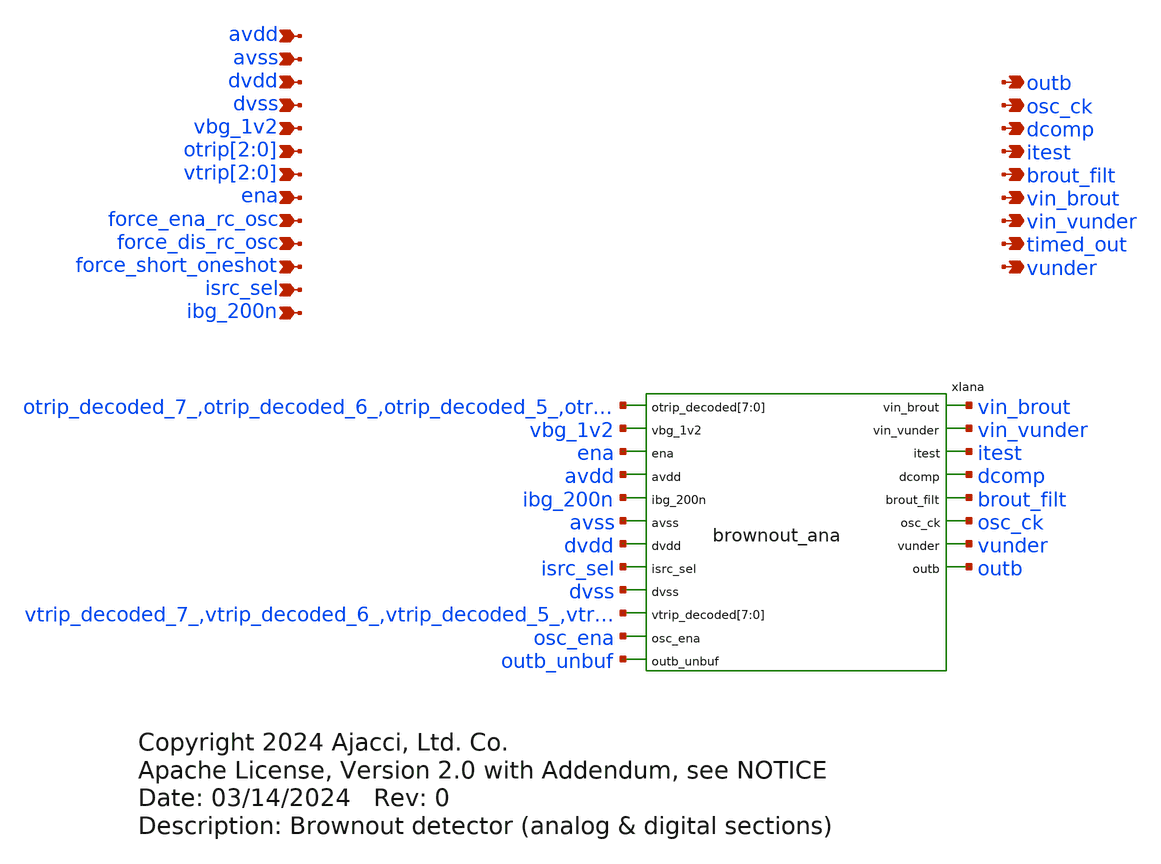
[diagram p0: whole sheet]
** sch_path: xschem/sky130_ajc_ip__brownout_sim.sch
* Copyright 2024 Ajacci, Ltd. Co.
* Apache License, Version 2.0 with Addendum, see NOTICE
**.subckt sky130_ajc_ip__brownout_sim avdd avss dvdd dvss vbg_1v2 otrip[2],otrip[1],otrip[0] ena
*+ force_dis_rc_osc force_short_oneshot isrc_sel ibg_200n vin_brout outb osc_ck brout_filt itest timed_out
*+ vtrip[2],vtrip[1],vtrip[0] vin_vunder vunder force_ena_rc_osc dcomp
*.ipin avdd
*.ipin avss
*.ipin dvdd
*.ipin dvss
*.ipin vbg_1v2
*.ipin otrip[2],otrip[1],otrip[0]
*.ipin ena
*.ipin force_dis_rc_osc
*.ipin force_short_oneshot
*.ipin isrc_sel
*.ipin ibg_200n
*.opin vin_brout
*.opin outb
*.opin osc_ck
*.opin brout_filt
*.opin itest
*.opin timed_out
*.ipin vtrip[2],vtrip[1],vtrip[0]
*.opin vin_vunder
*.opin vunder
*.ipin force_ena_rc_osc
*.opin dcomp
xIana vin_brout otrip_decoded_7_ otrip_decoded_6_ otrip_decoded_5_ otrip_decoded_4_ otrip_decoded_3_
+ otrip_decoded_2_ otrip_decoded_1_ otrip_decoded_0_ vin_vunder vbg_1v2 ena avdd ibg_200n itest avss dvdd isrc_sel
+ dvss vtrip_decoded_7_ vtrip_decoded_6_ vtrip_decoded_5_ vtrip_decoded_4_ vtrip_decoded_3_
+ vtrip_decoded_2_ vtrip_decoded_1_ vtrip_decoded_0_ dcomp brout_filt osc_ck osc_ena vunder outb outb_unbuf
+ brownout_ana
**** begin user architecture code



r0 otrip[0] otrip0 1
r1 otrip[1] otrip1 1
r2 otrip[2] otrip2 1
r3 vtrip[0] vtrip0 1
r4 vtrip[1] vtrip1 1
r5 vtrip[2] vtrip2 1

*XSPICE CO-SIM netlist
.include brownout_dig.out.spice
xibrownout_dig dvss dvdd brout_filt dcomp ena force_dis_rc_osc force_ena_rc_osc force_short_oneshot
+ osc_ck osc_ena  otrip0 otrip1 otrip2 otrip_decoded_0_ otrip_decoded_1_ otrip_decoded_2_ otrip_decoded_3_
+ otrip_decoded_4_ otrip_decoded_5_ otrip_decoded_6_ otrip_decoded_7_ outb_unbuf timed_out vtrip0 vtrip1 vtrip2
+ vtrip_decoded_0_ vtrip_decoded_1_ vtrip_decoded_2_ vtrip_decoded_3_ vtrip_decoded_4_ vtrip_decoded_5_
+ vtrip_decoded_6_ vtrip_decoded_7_ brownout_dig


**** end user architecture code
**.ends
.end
